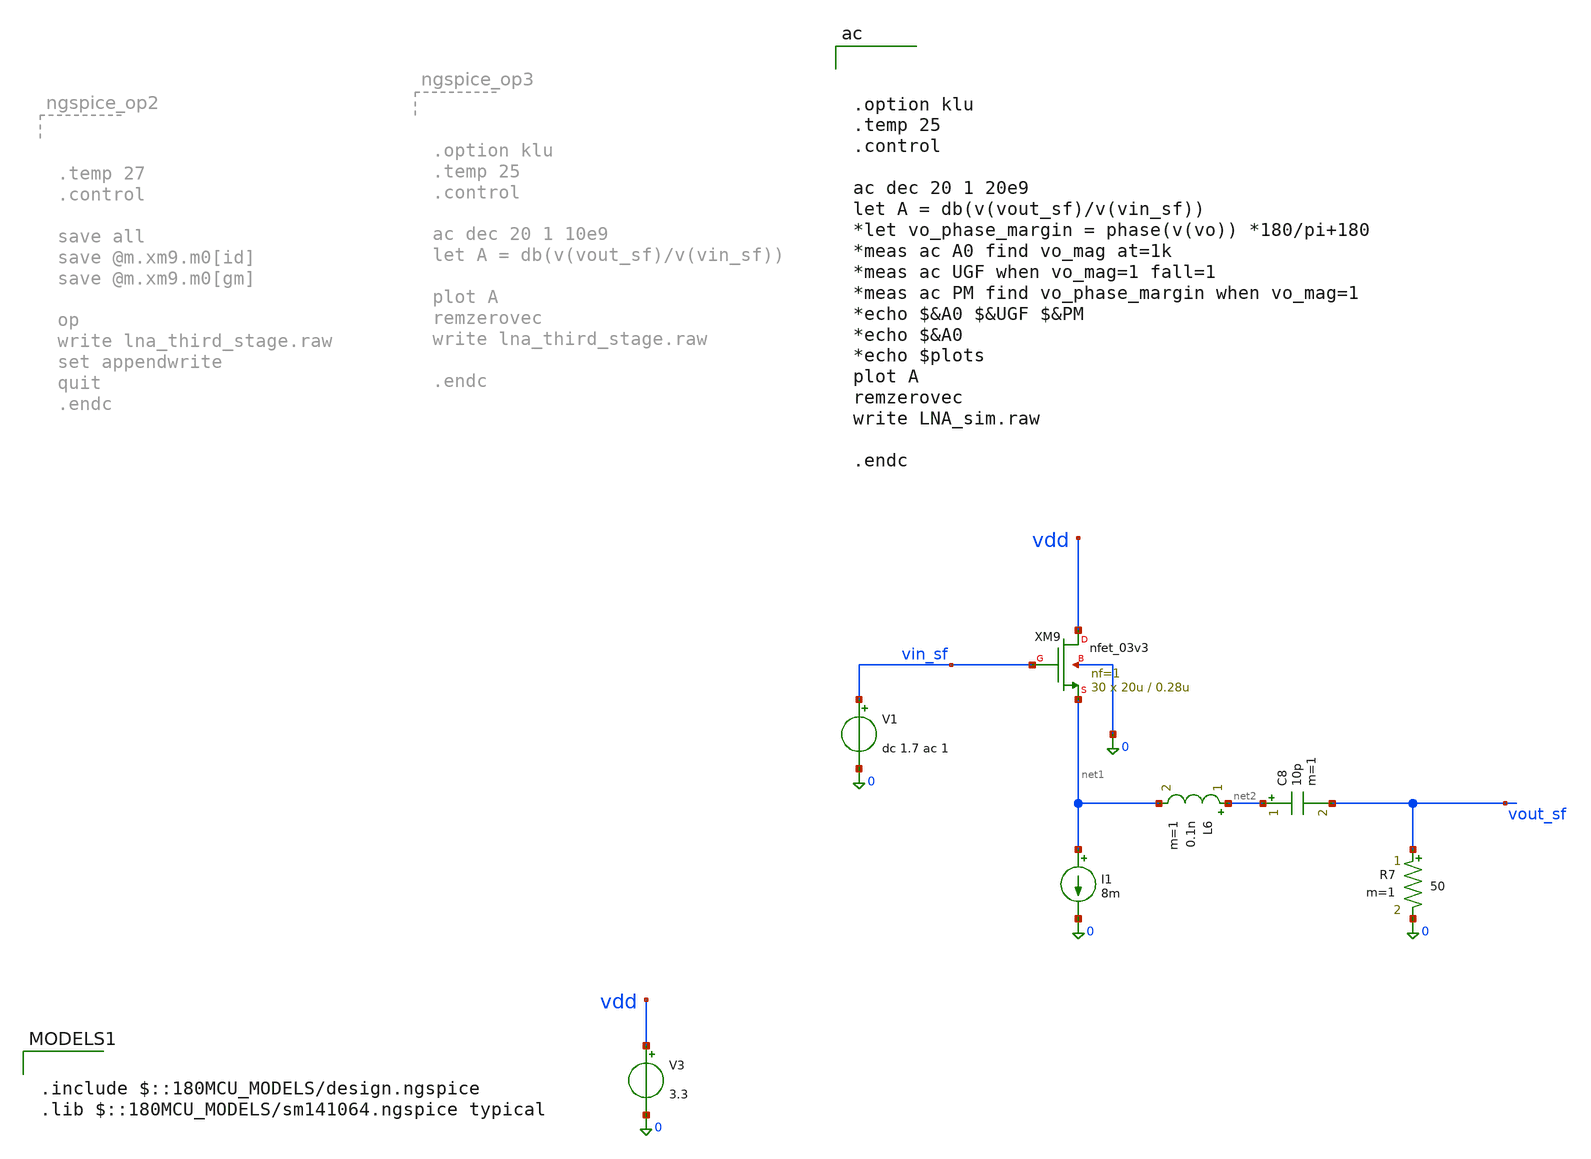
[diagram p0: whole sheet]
** sch_path: xschem/lna_third_stage.sch
**.subckt lna_third_stage
XM9 vdd vin_sf net1 0 nfet_03v3 L=0.28u W=20u nf=1 ad='int((nf+1)/2) * W/nf * 0.18u' as='int((nf+2)/2) * W/nf * 0.18u'
+ pd='2*int((nf+1)/2) * (W/nf + 0.18u)' ps='2*int((nf+2)/2) * (W/nf + 0.18u)' nrd='0.18u / W' nrs='0.18u / W'
+ sa=0 sb=0 sd=0 m=30
R7 vout_sf 0 50 m=1
V3 vdd 0 3.3
V1 vin_sf 0 dc 1.7 ac 1
I1 net1 0 8m
C8 net2 vout_sf 10p m=1
L6 net2 net1 0.1n m=1
**** begin user architecture code

.include $::180MCU_MODELS/design.ngspice
.lib $::180MCU_MODELS/sm141064.ngspice typical




.option klu
.temp 25
.control

ac dec 20 1 20e9
let A = db(v(vout_sf)/v(vin_sf))
*let vo_phase_margin = phase(v(vo)) *180/pi+180
*meas ac A0 find vo_mag at=1k
*meas ac UGF when vo_mag=1 fall=1
*meas ac PM find vo_phase_margin when vo_mag=1
*echo $&A0 $&UGF $&PM
*echo $&A0
*echo $plots
plot A
remzerovec
write LNA_sim.raw

.endc


**** end user architecture code
**.ends
.end
